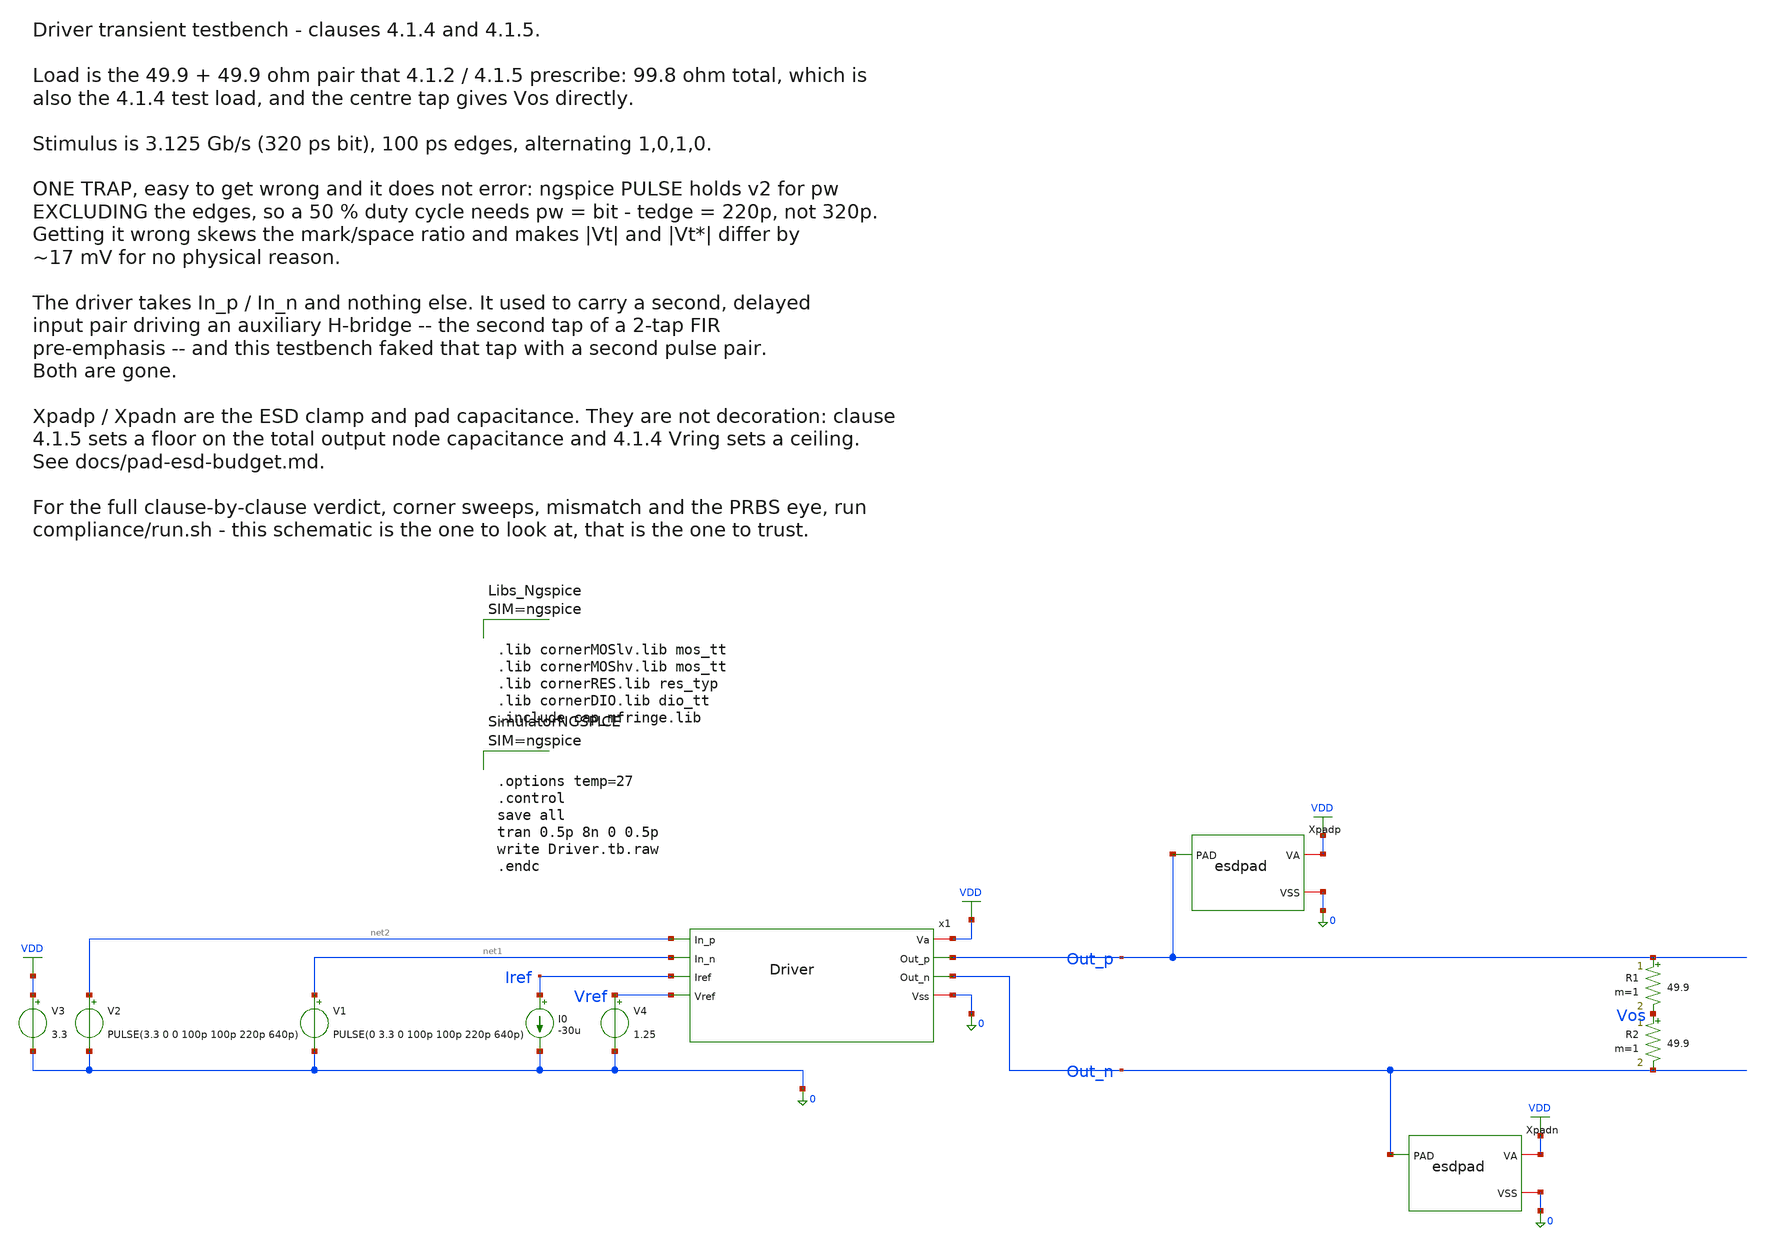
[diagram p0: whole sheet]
** sch_path: macros/lvds_tx/testbenches/xschem/Driver.tb.sch
**.subckt Driver.tb
x1 VDD Out_p net2 net1 Iref Vref Out_n 0 Driver
Xpadp Out_p VDD 0 esdpad
Xpadn Out_n VDD 0 esdpad
R1 Out_p Vos 49.9 m=1
R2 Vos Out_n 49.9 m=1
I0 Iref 0 -30u
V1 net1 0 PULSE(0 3.3 0 100p 100p 220p 640p)
V2 net2 0 PULSE(3.3 0 0 100p 100p 220p 640p)
V3 VDD 0 3.3
V4 Vref 0 1.25
**** begin user architecture code



.lib cornerMOSlv.lib mos_tt
.lib cornerMOShv.lib mos_tt
.lib cornerRES.lib res_typ
.lib cornerDIO.lib dio_tt
.include cap_mfringe.lib






.options temp=27
.control
save all
tran 0.5p 8n 0 0.5p
write Driver.tb.raw
.endc



**** end user architecture code
**.ends

* expanding   symbol:  Driver.sym # of pins=8
** sym_path: macros/lvds_tx/schematic/xschem/Driver.sym
** sch_path: macros/lvds_tx/schematic/xschem/Driver.sch
.subckt Driver Va Out_p In_p In_n Iref Vref Out_n Vss
*.iopin Va
*.iopin Vss
*.opin Out_p
*.opin Out_n
*.ipin In_p
*.ipin In_n
*.ipin Iref
*.ipin Vref
XCtn1 Va tail_n Va Va sg13_hv_pmos w=11.8u l=5.25u ng=2 m=1 mm_ok=1
XCtn2 Va tail_n Va Va sg13_hv_pmos w=5.7u l=5.8u ng=2 m=1 mm_ok=1
XM2 tail_p cmfb Va Va sg13_hv_pmos w=97.2u l=0.5u ng=20 m=1 mm_ok=1
XM5 Out_p In_p tail_p Va sg13_hv_pmos w=80u l=0.4u ng=16 m=1 mm_ok=1
XM4 Out_n In_n tail_p Va sg13_hv_pmos w=80u l=0.4u ng=16 m=1 mm_ok=1
XM1 Out_p In_p tail_n Vss sg13_hv_nmos w=30u l=0.45u ng=15 m=1 mm_ok=1
XM3 Out_n In_n tail_n Vss sg13_hv_nmos w=30u l=0.45u ng=15 m=1 mm_ok=1
XM6 tail_n Iref Vss Vss sg13_hv_nmos w=49.6u l=0.5u ng=31 m=2 mm_ok=1
XM9 Iref Iref Vss Vss sg13_hv_nmos w=0.8u l=0.5u ng=1 m=1 mm_ok=1
XM13 pd pd Va Va sg13_hv_pmos w=5u l=1u ng=1 m=1 mm_ok=1
XM14 cmfb pd Va Va sg13_hv_pmos w=5u l=1u ng=1 m=1 mm_ok=1
XM11 pd cm otail Vss sg13_hv_nmos w=40u l=1u ng=16 m=1 mm_ok=1
XM12 cmfb Vref otail Vss sg13_hv_nmos w=40u l=1u ng=16 m=1 mm_ok=1
XM10 otail Iref Vss Vss sg13_hv_nmos w=0.8u l=0.5u ng=1 m=1 mm_ok=1
XCc Va cc_g Va Va sg13_hv_pmos w=50u l=5u ng=10 m=1 mm_ok=1
XRc cmfb cc_g Vss rppd w=1u l=6u m=1 b=0 mm_ok=1
XRp Out_p cm Vss rhigh w=1u l=7.35u m=1 b=0 mm_ok=1
XRn Out_n cm Vss rhigh w=1u l=7.35u m=1 b=0 mm_ok=1
XCxp Out_p In_n cap_cmomf w=5.913u l=5.913u mmin=1 mmax=4 subblock=0 rfmodel=0 subscale=1 m=1
+ mm_ok=1
XCxn Out_n In_p cap_cmomf w=5.913u l=5.913u mmin=1 mmax=4 subblock=0 rfmodel=0 subscale=1 m=1
+ mm_ok=1
XCop Vss Out_p Vss Vss sg13_hv_nmos w=10u l=5u ng=1 m=2 mm_ok=1
XCon Vss Out_n Vss Vss sg13_hv_nmos w=10u l=5u ng=1 m=2 mm_ok=1
.ends


* expanding   symbol:  esdpad.sym # of pins=3
** sym_path: macros/lvds_tx/schematic/xschem/esdpad.sym
** sch_path: macros/lvds_tx/schematic/xschem/esdpad.sch
.subckt esdpad PAD VA VSS
*.iopin PAD
*.iopin VA
*.iopin VSS
XDdvdd VA PAD VSS diodevdd_4kv m=1
XDdvss VA PAD VSS diodevss_4kv m=1
Cpad PAD VSS 90f m=1
.ends

.GLOBAL VDD
.end
